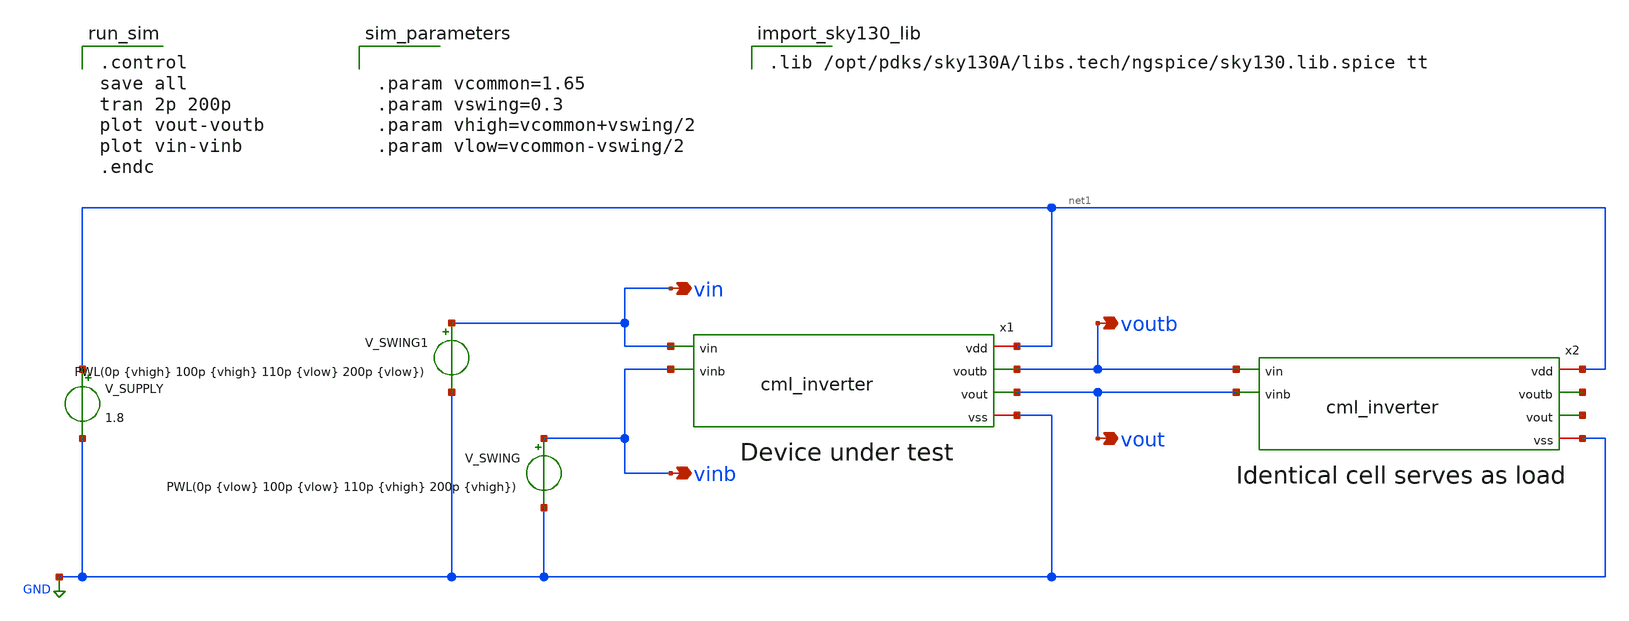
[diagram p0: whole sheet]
** sch_path: xschem/cml_inverter_tb.sch
**.subckt cml_inverter_tb voutb vout vin vinb
*.opin voutb
*.opin vout
*.opin vin
*.opin vinb
x1 net1 voutb vout vin vinb GND cml_inverter
V_SUPPLY net1 GND 1.8
V_SWING vinb GND PWL(0p {vlow} 100p {vlow} 110p {vhigh} 200p {vhigh})
x2 net1 net2 net3 voutb vout GND cml_inverter
V_SWING1 vin GND PWL(0p {vhigh} 100p {vhigh} 110p {vlow} 200p {vlow})
**** begin user architecture code

.control
save all
tran 2p 200p
plot vout-voutb
plot vin-vinb
.endc


.lib /opt/pdks/sky130A/libs.tech/ngspice/sky130.lib.spice tt



.param vcommon=1.65
.param vswing=0.3
.param vhigh=vcommon+vswing/2
.param vlow=vcommon-vswing/2


**** end user architecture code
**.ends

* expanding   symbol:  cml_inverter.sym # of pins=6
** sym_path: xschem/cml_inverter.sym
** sch_path: xschem/cml_inverter.sch
.subckt cml_inverter vdd voutb vout vin vinb vss
*.ipin vinb
*.ipin vin
*.iopin vdd
*.iopin vss
*.opin vout
*.opin voutb
ISS net1 vss 1m
R1 vdd vout 300 m=1
R2 vdd voutb 300 m=1
XM1 vout vinb net1 vss sky130_fd_pr__nfet_01v8 L=0.15 W=20 nf=1 ad='int((nf+1)/2) * W/nf * 0.29' as='int((nf+2)/2) * W/nf * 0.29'
+ pd='2*int((nf+1)/2) * (W/nf + 0.29)' ps='2*int((nf+2)/2) * (W/nf + 0.29)' nrd='0.29 / W' nrs='0.29 / W'
+ sa=0 sb=0 sd=0 mult=1 m=1
XM2 voutb vin net1 vss sky130_fd_pr__nfet_01v8 L=0.15 W=20 nf=1 ad='int((nf+1)/2) * W/nf * 0.29' as='int((nf+2)/2) * W/nf * 0.29'
+ pd='2*int((nf+1)/2) * (W/nf + 0.29)' ps='2*int((nf+2)/2) * (W/nf + 0.29)' nrd='0.29 / W' nrs='0.29 / W'
+ sa=0 sb=0 sd=0 mult=1 m=1
.ends

.GLOBAL GND
.end
